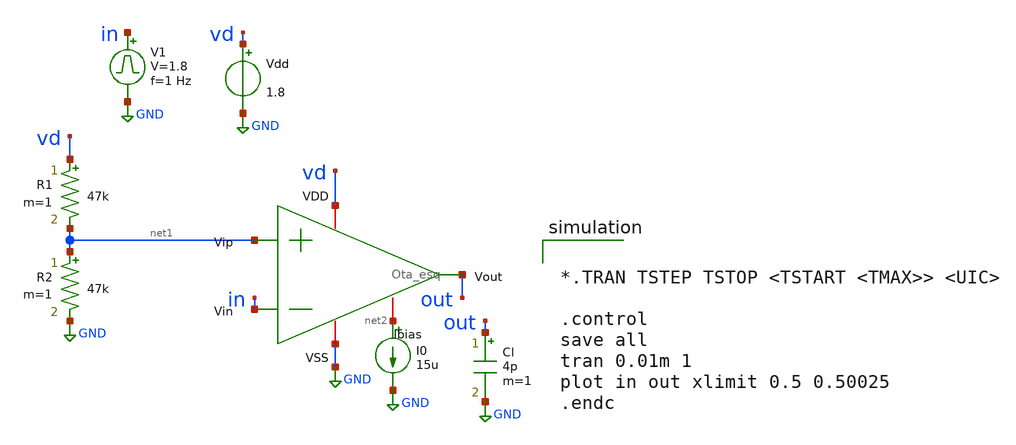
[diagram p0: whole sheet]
** sch_path: xschem/ota-tb-sw.sch
**.subckt ota-tb-sw
R1 vd net1 47k m=1
R2 net1 GND 47k m=1
Vdd vd GND 1.8
I0 net2 GND 15u
Cl out GND 4p m=1
x1 vd in net1 out net2 GND Ota_esq
V1 in GND pulse 0 1.8 '0.495/ 1 ' '0.01/1 ' '0.01/1 ' '0.49/1 ' '1/1 '
**** begin user architecture code

** opencircuitdesign pdks install
.lib $::SKYWATER_MODELS/sky130.lib.spice tt




*.TRAN TSTEP TSTOP <TSTART <TMAX>> <UIC>

.control
save all
tran 0.01m 1
plot in out xlimit 0.5 0.50025
.endc


**** end user architecture code
**.ends

* expanding   symbol:  Ota_esq.sym # of pins=6
** sym_path: Ota_esq.sym
** sch_path: Ota_esq.sch
.subckt Ota_esq VDD Vin Vip Vout Ibias VSS
*.ipin Vin
*.ipin Vip
*.iopin VDD
*.iopin VSS
*.iopin Ibias
*.opin Vout
XM1 net1 Vin net3 net3 sky130_fd_pr__pfet_01v8 L=0.25 W=2.899 nf=1 ad='int((nf+1)/2) * W/nf * 0.29' as='int((nf+2)/2) * W/nf * 0.29'
+ pd='2*int((nf+1)/2) * (W/nf + 0.29)' ps='2*int((nf+2)/2) * (W/nf + 0.29)' nrd='0.29 / W' nrs='0.29 / W'
+ sa=0 sb=0 sd=0 mult=1 m=1
XM2 net2 Vip net3 net3 sky130_fd_pr__pfet_01v8 L=0.25 W=2.899 nf=1 ad='int((nf+1)/2) * W/nf * 0.29' as='int((nf+2)/2) * W/nf * 0.29'
+ pd='2*int((nf+1)/2) * (W/nf + 0.29)' ps='2*int((nf+2)/2) * (W/nf + 0.29)' nrd='0.29 / W' nrs='0.29 / W'
+ sa=0 sb=0 sd=0 mult=1 m=1
XM3 net1 net1 VSS VSS sky130_fd_pr__nfet_01v8 L=0.25 W=0.667 nf=1 ad='int((nf+1)/2) * W/nf * 0.29' as='int((nf+2)/2) * W/nf * 0.29'
+ pd='2*int((nf+1)/2) * (W/nf + 0.29)' ps='2*int((nf+2)/2) * (W/nf + 0.29)' nrd='0.29 / W' nrs='0.29 / W'
+ sa=0 sb=0 sd=0 mult=1 m=1
XM4 net2 net1 VSS VSS sky130_fd_pr__nfet_01v8 L=0.25 W=0.667 nf=1 ad='int((nf+1)/2) * W/nf * 0.29' as='int((nf+2)/2) * W/nf * 0.29'
+ pd='2*int((nf+1)/2) * (W/nf + 0.29)' ps='2*int((nf+2)/2) * (W/nf + 0.29)' nrd='0.29 / W' nrs='0.29 / W'
+ sa=0 sb=0 sd=0 mult=1 m=1
XM5 net3 Ibias VDD VDD sky130_fd_pr__pfet_01v8 L=0.25 W=3.333 nf=1 ad='int((nf+1)/2) * W/nf * 0.29' as='int((nf+2)/2) * W/nf * 0.29'
+ pd='2*int((nf+1)/2) * (W/nf + 0.29)' ps='2*int((nf+2)/2) * (W/nf + 0.29)' nrd='0.29 / W' nrs='0.29 / W'
+ sa=0 sb=0 sd=0 mult=1 m=1
XM8 Ibias Ibias VDD VDD sky130_fd_pr__pfet_01v8 L=0.25 W=3.333 nf=1 ad='int((nf+1)/2) * W/nf * 0.29'
+ as='int((nf+2)/2) * W/nf * 0.29' pd='2*int((nf+1)/2) * (W/nf + 0.29)' ps='2*int((nf+2)/2) * (W/nf + 0.29)'
+ nrd='0.29 / W' nrs='0.29 / W' sa=0 sb=0 sd=0 mult=1 m=1
XM6 Vout Ibias VDD VDD sky130_fd_pr__pfet_01v8 L=0.25 W=17.279 nf=1 ad='int((nf+1)/2) * W/nf * 0.29'
+ as='int((nf+2)/2) * W/nf * 0.29' pd='2*int((nf+1)/2) * (W/nf + 0.29)' ps='2*int((nf+2)/2) * (W/nf + 0.29)'
+ nrd='0.29 / W' nrs='0.29 / W' sa=0 sb=0 sd=0 mult=1 m=1
XM7 Vout net2 VSS VSS sky130_fd_pr__nfet_01v8 L=0.25 W=6.192 nf=1 ad='int((nf+1)/2) * W/nf * 0.29' as='int((nf+2)/2) * W/nf * 0.29'
+ pd='2*int((nf+1)/2) * (W/nf + 0.29)' ps='2*int((nf+2)/2) * (W/nf + 0.29)' nrd='0.29 / W' nrs='0.29 / W'
+ sa=0 sb=0 sd=0 mult=1 m=1
XC1 net2 Vout sky130_fd_pr__cap_mim_m3_1 W=23 L=23 MF=1 m=1
.ends

.GLOBAL GND
.end
